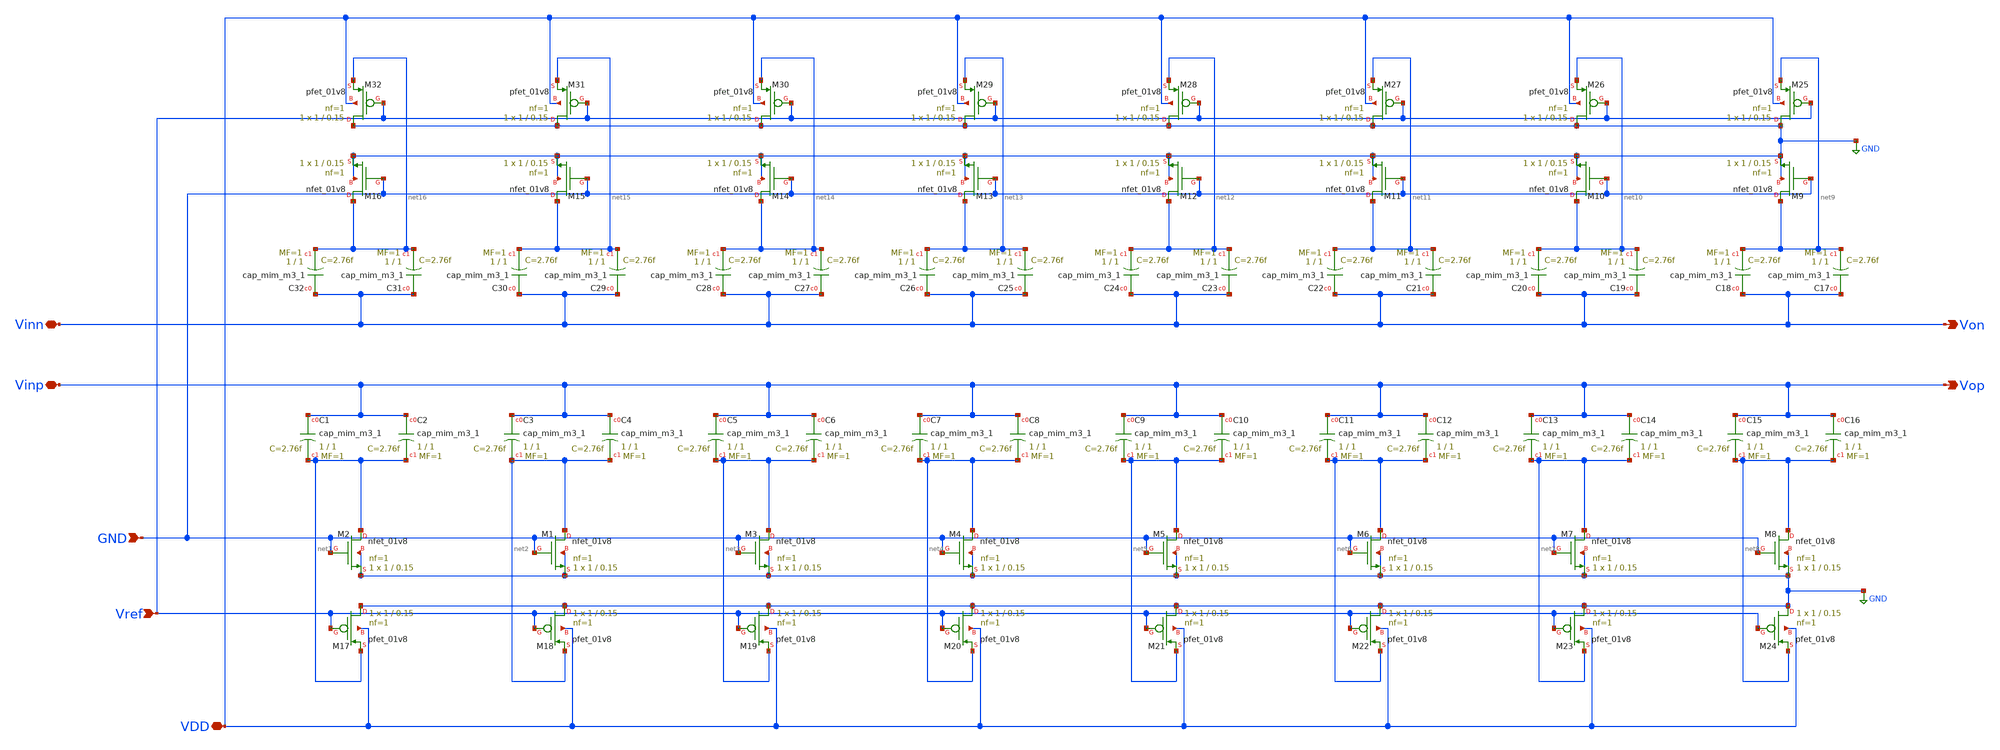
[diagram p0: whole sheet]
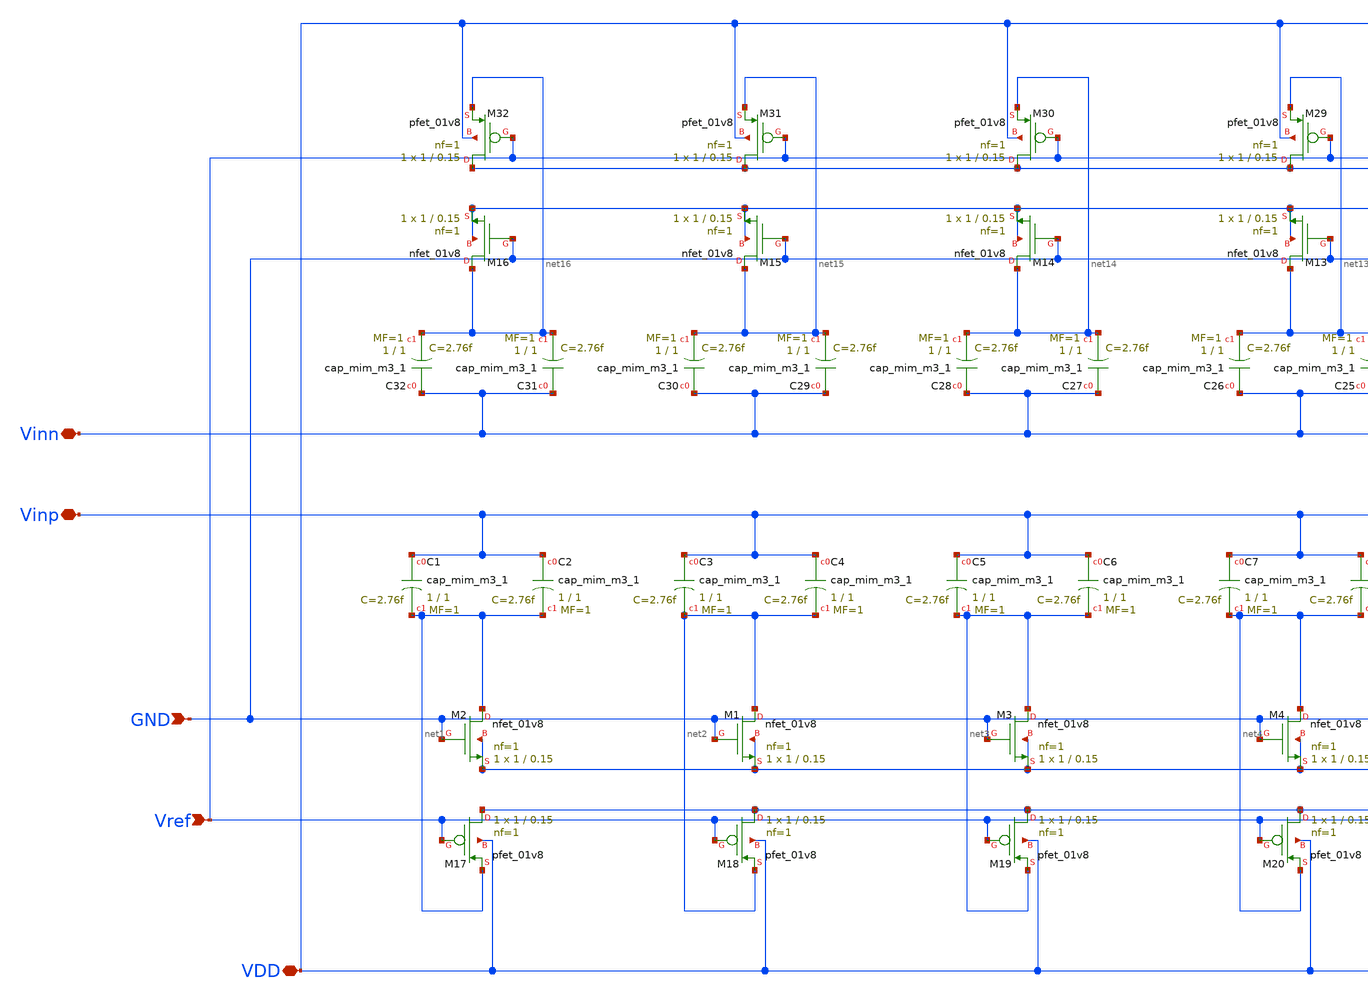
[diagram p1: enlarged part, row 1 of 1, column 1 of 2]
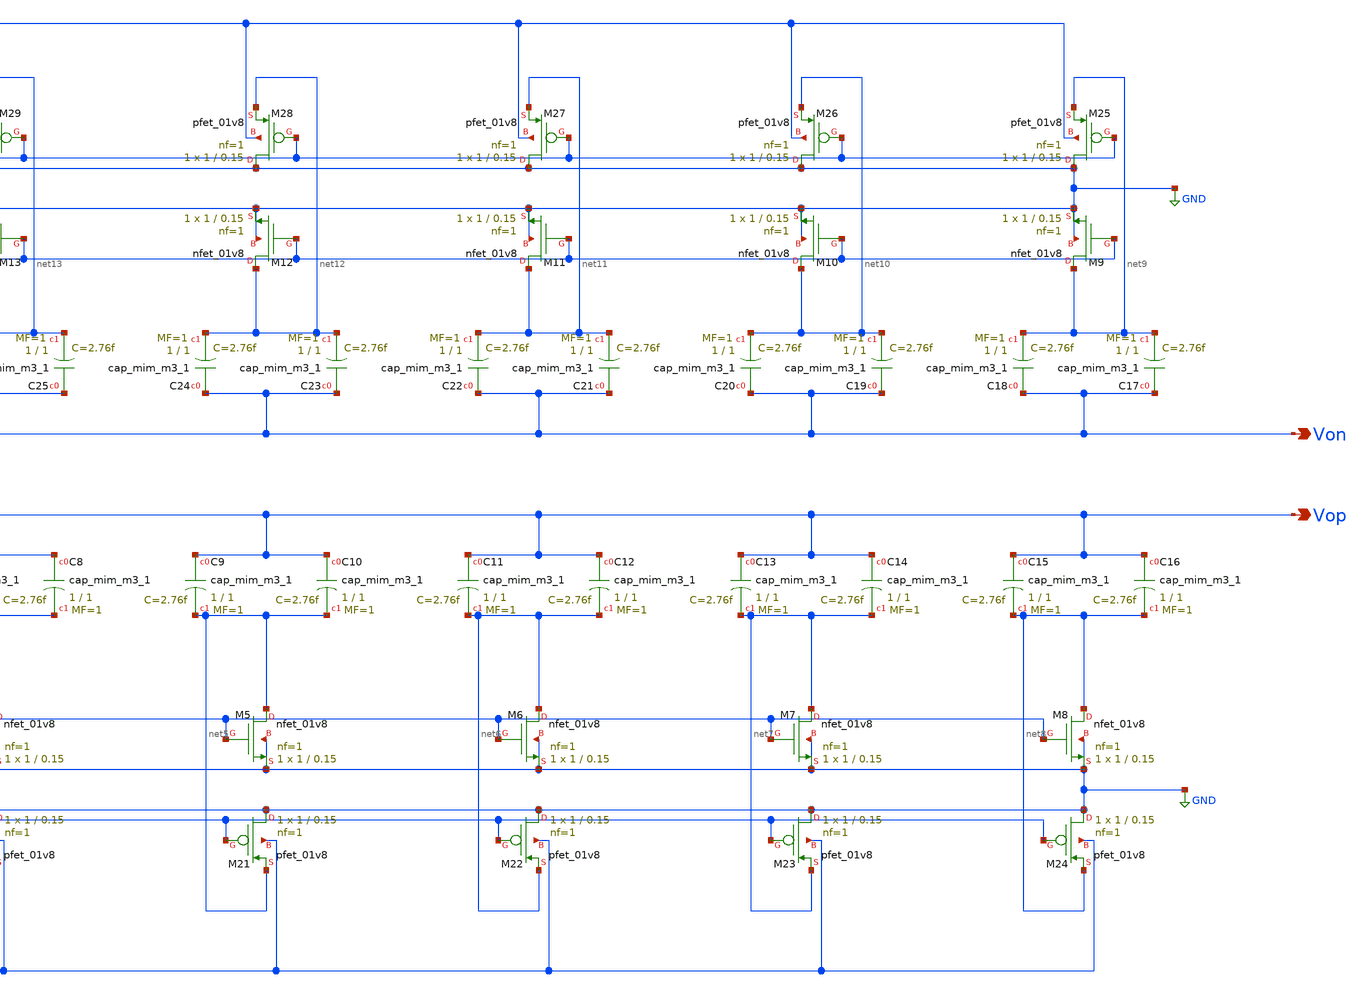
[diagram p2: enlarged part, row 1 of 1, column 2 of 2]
** sch_path: sar-adc/updated/CDAC.sch
**.subckt CDAC GND Vref VDD Vinn Vinp Von Vop
*.ipin GND
*.ipin Vref
*.iopin VDD
*.iopin Vinn
*.iopin Vinp
*.opin Von
*.opin Vop
XC1 Vinp net1 sky130_fd_pr__cap_mim_m3_1 W=1 L=1 MF=1 m=1
XC2 Vinp net1 sky130_fd_pr__cap_mim_m3_1 W=1 L=1 MF=1 m=1
XC3 Vinp net2 sky130_fd_pr__cap_mim_m3_1 W=1 L=1 MF=1 m=1
XC4 Vinp net2 sky130_fd_pr__cap_mim_m3_1 W=1 L=1 MF=1 m=1
XC5 Vinp net3 sky130_fd_pr__cap_mim_m3_1 W=1 L=1 MF=1 m=1
XC6 Vinp net3 sky130_fd_pr__cap_mim_m3_1 W=1 L=1 MF=1 m=1
XC7 Vinp net4 sky130_fd_pr__cap_mim_m3_1 W=1 L=1 MF=1 m=1
XC8 Vinp net4 sky130_fd_pr__cap_mim_m3_1 W=1 L=1 MF=1 m=1
XC9 Vinp net5 sky130_fd_pr__cap_mim_m3_1 W=1 L=1 MF=1 m=1
XC10 Vinp net5 sky130_fd_pr__cap_mim_m3_1 W=1 L=1 MF=1 m=1
XC11 Vinp net6 sky130_fd_pr__cap_mim_m3_1 W=1 L=1 MF=1 m=1
XC12 Vinp net6 sky130_fd_pr__cap_mim_m3_1 W=1 L=1 MF=1 m=1
XC13 Vinp net7 sky130_fd_pr__cap_mim_m3_1 W=1 L=1 MF=1 m=1
XC14 Vinp net7 sky130_fd_pr__cap_mim_m3_1 W=1 L=1 MF=1 m=1
XC15 Vinp net8 sky130_fd_pr__cap_mim_m3_1 W=1 L=1 MF=1 m=1
XC16 Vinp net8 sky130_fd_pr__cap_mim_m3_1 W=1 L=1 MF=1 m=1
XC17 Vinn net9 sky130_fd_pr__cap_mim_m3_1 W=1 L=1 MF=1 m=1
XC18 Vinn net9 sky130_fd_pr__cap_mim_m3_1 W=1 L=1 MF=1 m=1
XC19 Vinn net10 sky130_fd_pr__cap_mim_m3_1 W=1 L=1 MF=1 m=1
XC20 Vinn net10 sky130_fd_pr__cap_mim_m3_1 W=1 L=1 MF=1 m=1
XC21 Vinn net11 sky130_fd_pr__cap_mim_m3_1 W=1 L=1 MF=1 m=1
XC22 Vinn net11 sky130_fd_pr__cap_mim_m3_1 W=1 L=1 MF=1 m=1
XC23 Vinn net12 sky130_fd_pr__cap_mim_m3_1 W=1 L=1 MF=1 m=1
XC24 Vinn net12 sky130_fd_pr__cap_mim_m3_1 W=1 L=1 MF=1 m=1
XC25 Vinn net13 sky130_fd_pr__cap_mim_m3_1 W=1 L=1 MF=1 m=1
XC26 Vinn net13 sky130_fd_pr__cap_mim_m3_1 W=1 L=1 MF=1 m=1
XC27 Vinn net14 sky130_fd_pr__cap_mim_m3_1 W=1 L=1 MF=1 m=1
XC28 Vinn net14 sky130_fd_pr__cap_mim_m3_1 W=1 L=1 MF=1 m=1
XC29 Vinn net15 sky130_fd_pr__cap_mim_m3_1 W=1 L=1 MF=1 m=1
XC30 Vinn net15 sky130_fd_pr__cap_mim_m3_1 W=1 L=1 MF=1 m=1
XC31 Vinn net16 sky130_fd_pr__cap_mim_m3_1 W=1 L=1 MF=1 m=1
XC32 Vinn net16 sky130_fd_pr__cap_mim_m3_1 W=1 L=1 MF=1 m=1
XM2 net1 GND GND GND sky130_fd_pr__nfet_01v8 L=0.15 W=1 nf=1 ad='int((1 + 1)/2) * 1 / 1 * 0.29' as='int((1 + 2)/2) * 1 / 1 * 0.29'
+ pd='2*int((1 + 1)/2) * (1 / 1 + 0.29)' ps='2*int((1 + 2)/2) * (1 / 1 + 0.29)' nrd='0.29 / 1 ' nrs='0.29 / 1 '
+ sa=0 sb=0 sd=0 mult=1 m=1
XM1 net2 GND GND GND sky130_fd_pr__nfet_01v8 L=0.15 W=1 nf=1 ad='int((1 + 1)/2) * 1 / 1 * 0.29' as='int((1 + 2)/2) * 1 / 1 * 0.29'
+ pd='2*int((1 + 1)/2) * (1 / 1 + 0.29)' ps='2*int((1 + 2)/2) * (1 / 1 + 0.29)' nrd='0.29 / 1 ' nrs='0.29 / 1 '
+ sa=0 sb=0 sd=0 mult=1 m=1
XM3 net3 GND GND GND sky130_fd_pr__nfet_01v8 L=0.15 W=1 nf=1 ad='int((1 + 1)/2) * 1 / 1 * 0.29' as='int((1 + 2)/2) * 1 / 1 * 0.29'
+ pd='2*int((1 + 1)/2) * (1 / 1 + 0.29)' ps='2*int((1 + 2)/2) * (1 / 1 + 0.29)' nrd='0.29 / 1 ' nrs='0.29 / 1 '
+ sa=0 sb=0 sd=0 mult=1 m=1
XM4 net4 GND GND GND sky130_fd_pr__nfet_01v8 L=0.15 W=1 nf=1 ad='int((1 + 1)/2) * 1 / 1 * 0.29' as='int((1 + 2)/2) * 1 / 1 * 0.29'
+ pd='2*int((1 + 1)/2) * (1 / 1 + 0.29)' ps='2*int((1 + 2)/2) * (1 / 1 + 0.29)' nrd='0.29 / 1 ' nrs='0.29 / 1 '
+ sa=0 sb=0 sd=0 mult=1 m=1
XM5 net5 GND GND GND sky130_fd_pr__nfet_01v8 L=0.15 W=1 nf=1 ad='int((1 + 1)/2) * 1 / 1 * 0.29' as='int((1 + 2)/2) * 1 / 1 * 0.29'
+ pd='2*int((1 + 1)/2) * (1 / 1 + 0.29)' ps='2*int((1 + 2)/2) * (1 / 1 + 0.29)' nrd='0.29 / 1 ' nrs='0.29 / 1 '
+ sa=0 sb=0 sd=0 mult=1 m=1
XM6 net6 GND GND GND sky130_fd_pr__nfet_01v8 L=0.15 W=1 nf=1 ad='int((1 + 1)/2) * 1 / 1 * 0.29' as='int((1 + 2)/2) * 1 / 1 * 0.29'
+ pd='2*int((1 + 1)/2) * (1 / 1 + 0.29)' ps='2*int((1 + 2)/2) * (1 / 1 + 0.29)' nrd='0.29 / 1 ' nrs='0.29 / 1 '
+ sa=0 sb=0 sd=0 mult=1 m=1
XM7 net7 GND GND GND sky130_fd_pr__nfet_01v8 L=0.15 W=1 nf=1 ad='int((1 + 1)/2) * 1 / 1 * 0.29' as='int((1 + 2)/2) * 1 / 1 * 0.29'
+ pd='2*int((1 + 1)/2) * (1 / 1 + 0.29)' ps='2*int((1 + 2)/2) * (1 / 1 + 0.29)' nrd='0.29 / 1 ' nrs='0.29 / 1 '
+ sa=0 sb=0 sd=0 mult=1 m=1
XM8 net8 GND GND GND sky130_fd_pr__nfet_01v8 L=0.15 W=1 nf=1 ad='int((1 + 1)/2) * 1 / 1 * 0.29' as='int((1 + 2)/2) * 1 / 1 * 0.29'
+ pd='2*int((1 + 1)/2) * (1 / 1 + 0.29)' ps='2*int((1 + 2)/2) * (1 / 1 + 0.29)' nrd='0.29 / 1 ' nrs='0.29 / 1 '
+ sa=0 sb=0 sd=0 mult=1 m=1
XM9 net9 GND GND GND sky130_fd_pr__nfet_01v8 L=0.15 W=1 nf=1 ad='int((1 + 1)/2) * 1 / 1 * 0.29' as='int((1 + 2)/2) * 1 / 1 * 0.29'
+ pd='2*int((1 + 1)/2) * (1 / 1 + 0.29)' ps='2*int((1 + 2)/2) * (1 / 1 + 0.29)' nrd='0.29 / 1 ' nrs='0.29 / 1 '
+ sa=0 sb=0 sd=0 mult=1 m=1
XM10 net10 GND GND GND sky130_fd_pr__nfet_01v8 L=0.15 W=1 nf=1 ad='int((1 + 1)/2) * 1 / 1 * 0.29' as='int((1 + 2)/2) * 1 / 1 * 0.29'
+ pd='2*int((1 + 1)/2) * (1 / 1 + 0.29)' ps='2*int((1 + 2)/2) * (1 / 1 + 0.29)' nrd='0.29 / 1 ' nrs='0.29 / 1 '
+ sa=0 sb=0 sd=0 mult=1 m=1
XM11 net11 GND GND GND sky130_fd_pr__nfet_01v8 L=0.15 W=1 nf=1 ad='int((1 + 1)/2) * 1 / 1 * 0.29' as='int((1 + 2)/2) * 1 / 1 * 0.29'
+ pd='2*int((1 + 1)/2) * (1 / 1 + 0.29)' ps='2*int((1 + 2)/2) * (1 / 1 + 0.29)' nrd='0.29 / 1 ' nrs='0.29 / 1 '
+ sa=0 sb=0 sd=0 mult=1 m=1
XM12 net12 GND GND GND sky130_fd_pr__nfet_01v8 L=0.15 W=1 nf=1 ad='int((1 + 1)/2) * 1 / 1 * 0.29' as='int((1 + 2)/2) * 1 / 1 * 0.29'
+ pd='2*int((1 + 1)/2) * (1 / 1 + 0.29)' ps='2*int((1 + 2)/2) * (1 / 1 + 0.29)' nrd='0.29 / 1 ' nrs='0.29 / 1 '
+ sa=0 sb=0 sd=0 mult=1 m=1
XM13 net13 GND GND GND sky130_fd_pr__nfet_01v8 L=0.15 W=1 nf=1 ad='int((1 + 1)/2) * 1 / 1 * 0.29' as='int((1 + 2)/2) * 1 / 1 * 0.29'
+ pd='2*int((1 + 1)/2) * (1 / 1 + 0.29)' ps='2*int((1 + 2)/2) * (1 / 1 + 0.29)' nrd='0.29 / 1 ' nrs='0.29 / 1 '
+ sa=0 sb=0 sd=0 mult=1 m=1
XM14 net14 GND GND GND sky130_fd_pr__nfet_01v8 L=0.15 W=1 nf=1 ad='int((1 + 1)/2) * 1 / 1 * 0.29' as='int((1 + 2)/2) * 1 / 1 * 0.29'
+ pd='2*int((1 + 1)/2) * (1 / 1 + 0.29)' ps='2*int((1 + 2)/2) * (1 / 1 + 0.29)' nrd='0.29 / 1 ' nrs='0.29 / 1 '
+ sa=0 sb=0 sd=0 mult=1 m=1
XM15 net15 GND GND GND sky130_fd_pr__nfet_01v8 L=0.15 W=1 nf=1 ad='int((1 + 1)/2) * 1 / 1 * 0.29' as='int((1 + 2)/2) * 1 / 1 * 0.29'
+ pd='2*int((1 + 1)/2) * (1 / 1 + 0.29)' ps='2*int((1 + 2)/2) * (1 / 1 + 0.29)' nrd='0.29 / 1 ' nrs='0.29 / 1 '
+ sa=0 sb=0 sd=0 mult=1 m=1
XM16 net16 GND GND GND sky130_fd_pr__nfet_01v8 L=0.15 W=1 nf=1 ad='int((1 + 1)/2) * 1 / 1 * 0.29' as='int((1 + 2)/2) * 1 / 1 * 0.29'
+ pd='2*int((1 + 1)/2) * (1 / 1 + 0.29)' ps='2*int((1 + 2)/2) * (1 / 1 + 0.29)' nrd='0.29 / 1 ' nrs='0.29 / 1 '
+ sa=0 sb=0 sd=0 mult=1 m=1
XM17 GND Vref net1 VDD sky130_fd_pr__pfet_01v8 L=0.15 W=1 nf=1 ad='int((nf+1)/2) * W/nf * 0.29' as='int((nf+2)/2) * W/nf * 0.29'
+ pd='2*int((nf+1)/2) * (W/nf + 0.29)' ps='2*int((nf+2)/2) * (W/nf + 0.29)' nrd='0.29 / W' nrs='0.29 / W'
+ sa=0 sb=0 sd=0 mult=1 m=1
XM18 GND Vref net2 VDD sky130_fd_pr__pfet_01v8 L=0.15 W=1 nf=1 ad='int((nf+1)/2) * W/nf * 0.29' as='int((nf+2)/2) * W/nf * 0.29'
+ pd='2*int((nf+1)/2) * (W/nf + 0.29)' ps='2*int((nf+2)/2) * (W/nf + 0.29)' nrd='0.29 / W' nrs='0.29 / W'
+ sa=0 sb=0 sd=0 mult=1 m=1
XM19 GND Vref net3 VDD sky130_fd_pr__pfet_01v8 L=0.15 W=1 nf=1 ad='int((nf+1)/2) * W/nf * 0.29' as='int((nf+2)/2) * W/nf * 0.29'
+ pd='2*int((nf+1)/2) * (W/nf + 0.29)' ps='2*int((nf+2)/2) * (W/nf + 0.29)' nrd='0.29 / W' nrs='0.29 / W'
+ sa=0 sb=0 sd=0 mult=1 m=1
XM20 GND Vref net4 VDD sky130_fd_pr__pfet_01v8 L=0.15 W=1 nf=1 ad='int((nf+1)/2) * W/nf * 0.29' as='int((nf+2)/2) * W/nf * 0.29'
+ pd='2*int((nf+1)/2) * (W/nf + 0.29)' ps='2*int((nf+2)/2) * (W/nf + 0.29)' nrd='0.29 / W' nrs='0.29 / W'
+ sa=0 sb=0 sd=0 mult=1 m=1
XM21 GND Vref net5 VDD sky130_fd_pr__pfet_01v8 L=0.15 W=1 nf=1 ad='int((nf+1)/2) * W/nf * 0.29' as='int((nf+2)/2) * W/nf * 0.29'
+ pd='2*int((nf+1)/2) * (W/nf + 0.29)' ps='2*int((nf+2)/2) * (W/nf + 0.29)' nrd='0.29 / W' nrs='0.29 / W'
+ sa=0 sb=0 sd=0 mult=1 m=1
XM22 GND Vref net6 VDD sky130_fd_pr__pfet_01v8 L=0.15 W=1 nf=1 ad='int((nf+1)/2) * W/nf * 0.29' as='int((nf+2)/2) * W/nf * 0.29'
+ pd='2*int((nf+1)/2) * (W/nf + 0.29)' ps='2*int((nf+2)/2) * (W/nf + 0.29)' nrd='0.29 / W' nrs='0.29 / W'
+ sa=0 sb=0 sd=0 mult=1 m=1
XM23 GND Vref net7 VDD sky130_fd_pr__pfet_01v8 L=0.15 W=1 nf=1 ad='int((nf+1)/2) * W/nf * 0.29' as='int((nf+2)/2) * W/nf * 0.29'
+ pd='2*int((nf+1)/2) * (W/nf + 0.29)' ps='2*int((nf+2)/2) * (W/nf + 0.29)' nrd='0.29 / W' nrs='0.29 / W'
+ sa=0 sb=0 sd=0 mult=1 m=1
XM24 GND Vref net8 VDD sky130_fd_pr__pfet_01v8 L=0.15 W=1 nf=1 ad='int((nf+1)/2) * W/nf * 0.29' as='int((nf+2)/2) * W/nf * 0.29'
+ pd='2*int((nf+1)/2) * (W/nf + 0.29)' ps='2*int((nf+2)/2) * (W/nf + 0.29)' nrd='0.29 / W' nrs='0.29 / W'
+ sa=0 sb=0 sd=0 mult=1 m=1
XM25 GND Vref net9 VDD sky130_fd_pr__pfet_01v8 L=0.15 W=1 nf=1 ad='int((nf+1)/2) * W/nf * 0.29' as='int((nf+2)/2) * W/nf * 0.29'
+ pd='2*int((nf+1)/2) * (W/nf + 0.29)' ps='2*int((nf+2)/2) * (W/nf + 0.29)' nrd='0.29 / W' nrs='0.29 / W'
+ sa=0 sb=0 sd=0 mult=1 m=1
XM26 GND Vref net10 VDD sky130_fd_pr__pfet_01v8 L=0.15 W=1 nf=1 ad='int((nf+1)/2) * W/nf * 0.29' as='int((nf+2)/2) * W/nf * 0.29'
+ pd='2*int((nf+1)/2) * (W/nf + 0.29)' ps='2*int((nf+2)/2) * (W/nf + 0.29)' nrd='0.29 / W' nrs='0.29 / W'
+ sa=0 sb=0 sd=0 mult=1 m=1
XM27 GND Vref net11 VDD sky130_fd_pr__pfet_01v8 L=0.15 W=1 nf=1 ad='int((nf+1)/2) * W/nf * 0.29' as='int((nf+2)/2) * W/nf * 0.29'
+ pd='2*int((nf+1)/2) * (W/nf + 0.29)' ps='2*int((nf+2)/2) * (W/nf + 0.29)' nrd='0.29 / W' nrs='0.29 / W'
+ sa=0 sb=0 sd=0 mult=1 m=1
XM28 GND Vref net12 VDD sky130_fd_pr__pfet_01v8 L=0.15 W=1 nf=1 ad='int((nf+1)/2) * W/nf * 0.29' as='int((nf+2)/2) * W/nf * 0.29'
+ pd='2*int((nf+1)/2) * (W/nf + 0.29)' ps='2*int((nf+2)/2) * (W/nf + 0.29)' nrd='0.29 / W' nrs='0.29 / W'
+ sa=0 sb=0 sd=0 mult=1 m=1
XM29 GND Vref net13 VDD sky130_fd_pr__pfet_01v8 L=0.15 W=1 nf=1 ad='int((nf+1)/2) * W/nf * 0.29' as='int((nf+2)/2) * W/nf * 0.29'
+ pd='2*int((nf+1)/2) * (W/nf + 0.29)' ps='2*int((nf+2)/2) * (W/nf + 0.29)' nrd='0.29 / W' nrs='0.29 / W'
+ sa=0 sb=0 sd=0 mult=1 m=1
XM30 GND Vref net14 VDD sky130_fd_pr__pfet_01v8 L=0.15 W=1 nf=1 ad='int((nf+1)/2) * W/nf * 0.29' as='int((nf+2)/2) * W/nf * 0.29'
+ pd='2*int((nf+1)/2) * (W/nf + 0.29)' ps='2*int((nf+2)/2) * (W/nf + 0.29)' nrd='0.29 / W' nrs='0.29 / W'
+ sa=0 sb=0 sd=0 mult=1 m=1
XM31 GND Vref net15 VDD sky130_fd_pr__pfet_01v8 L=0.15 W=1 nf=1 ad='int((nf+1)/2) * W/nf * 0.29' as='int((nf+2)/2) * W/nf * 0.29'
+ pd='2*int((nf+1)/2) * (W/nf + 0.29)' ps='2*int((nf+2)/2) * (W/nf + 0.29)' nrd='0.29 / W' nrs='0.29 / W'
+ sa=0 sb=0 sd=0 mult=1 m=1
XM32 GND Vref net16 VDD sky130_fd_pr__pfet_01v8 L=0.15 W=1 nf=1 ad='int((nf+1)/2) * W/nf * 0.29' as='int((nf+2)/2) * W/nf * 0.29'
+ pd='2*int((nf+1)/2) * (W/nf + 0.29)' ps='2*int((nf+2)/2) * (W/nf + 0.29)' nrd='0.29 / W' nrs='0.29 / W'
+ sa=0 sb=0 sd=0 mult=1 m=1
**.ends
.GLOBAL GND
.end
